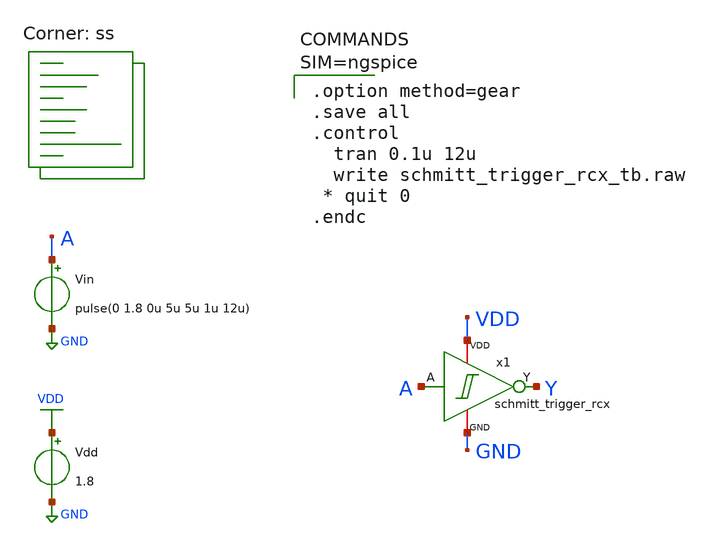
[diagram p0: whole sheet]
** sch_path: design/xschem/layout_tb/schmitt_trigger_rcx_tb.sch
**.subckt schmitt_trigger_rcx_tb
x1 A Y VDD GND schmitt_trigger_rcx
Vdd VDD GND 1.8
Vin A GND pulse(0 1.8 0u 5u 5u 1u 12u)
**** begin user architecture code


.option method=gear
.save all
.control
  tran 0.1u 12u
  write schmitt_trigger_rcx_tb.raw
 * quit 0
.endc


.lib $::SKYWATER_MODELS/sky130.lib.spice ss
**** end user architecture code
**.ends

* expanding   symbol:  schmitt_trigger_rcx.sym # of pins=4
** sym_path: design/xschem/schmitt_trigger.sym
.include [abs_sym_path schmitt_trigger_rcx.spice]
.GLOBAL VDD
.GLOBAL GND
.end
